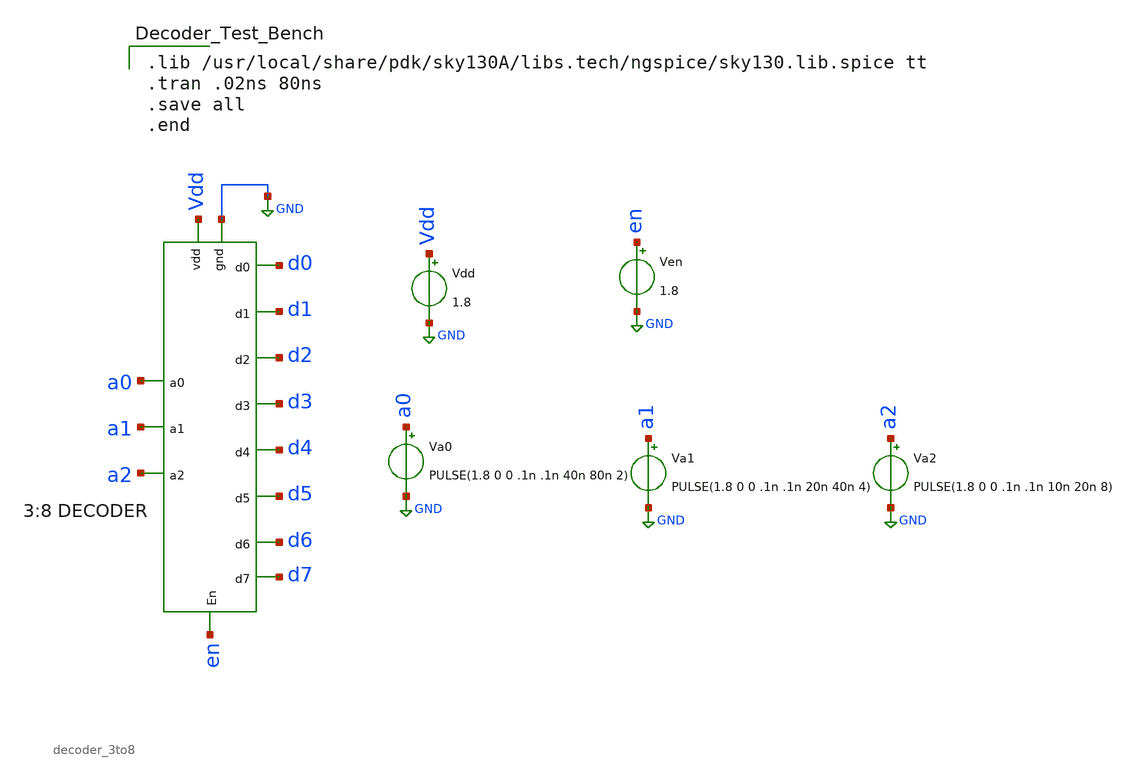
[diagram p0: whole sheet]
** sch_path: Projects/Schematic_Design_and_Analysis_of_an_8-Word_8-Bit_Static_RAM_with_6T_Storage_Cells_using_SKY130PDK/assets/schematic/decoder_3to8_tb.sch
**.subckt decoder_3to8_tb
Vdd Vdd GND 1.8
Va0 a0 GND PULSE(1.8 0 0 .1n .1n 40n 80n 2)
Va1 a1 GND PULSE(1.8 0 0 .1n .1n 20n 40n 4)
Va2 a2 GND PULSE(1.8 0 0 .1n .1n 10n 20n 8)
x1 d0 d1 d2 d3 d4 d5 d6 d7 Vdd GND en a0 a1 a2 decoder_3to8
Ven en GND 1.8
**** begin user architecture code

.lib /usr/local/share/pdk/sky130A/libs.tech/ngspice/sky130.lib.spice tt
.tran .02ns 80ns
.save all
.end

**** end user architecture code
**.ends

* expanding   symbol:  decoder_3to8.sym # of pins=14
** sym_path: Projects/Schematic_Design_and_Analysis_of_an_8-Word_8-Bit_Static_RAM_with_6T_Storage_Cells_using_SKY130PDK/assets/schematic/decoder_3to8.sym
** sch_path: Projects/Schematic_Design_and_Analysis_of_an_8-Word_8-Bit_Static_RAM_with_6T_Storage_Cells_using_SKY130PDK/assets/schematic/decoder_3to8.sch
.subckt decoder_3to8 d0 d1 d2 d3 d4 d5 d6 d7 vdd gnd En a0 a1 a2
*.ipin a0
*.ipin a1
*.ipin a2
*.opin d0
*.ipin vdd
*.ipin gnd
*.ipin En
*.opin d1
*.opin d2
*.opin d3
*.opin d4
*.opin d5
*.opin d6
*.opin d7
XM25 net1 a2 gnd gnd sky130_fd_pr__nfet_01v8 L=0.15 W=1 nf=1 ad='int((nf+1)/2) * W/nf * 0.29' as='int((nf+2)/2) * W/nf * 0.29'
+ pd='2*int((nf+1)/2) * (W/nf + 0.29)' ps='2*int((nf+2)/2) * (W/nf + 0.29)' nrd='0.29 / W' nrs='0.29 / W'
+ sa=0 sb=0 sd=0 mult=1 m=1
XM26 net1 a2 vdd vdd sky130_fd_pr__pfet_01v8 L=0.15 W=2 nf=1 ad='int((nf+1)/2) * W/nf * 0.29' as='int((nf+2)/2) * W/nf * 0.29'
+ pd='2*int((nf+1)/2) * (W/nf + 0.29)' ps='2*int((nf+2)/2) * (W/nf + 0.29)' nrd='0.29 / W' nrs='0.29 / W'
+ sa=0 sb=0 sd=0 mult=1 m=1
XM28 net2 a1 vdd vdd sky130_fd_pr__pfet_01v8 L=0.15 W=2 nf=1 ad='int((nf+1)/2) * W/nf * 0.29' as='int((nf+2)/2) * W/nf * 0.29'
+ pd='2*int((nf+1)/2) * (W/nf + 0.29)' ps='2*int((nf+2)/2) * (W/nf + 0.29)' nrd='0.29 / W' nrs='0.29 / W'
+ sa=0 sb=0 sd=0 mult=1 m=1
XM30 net3 a0 vdd vdd sky130_fd_pr__pfet_01v8 L=0.15 W=2 nf=1 ad='int((nf+1)/2) * W/nf * 0.29' as='int((nf+2)/2) * W/nf * 0.29'
+ pd='2*int((nf+1)/2) * (W/nf + 0.29)' ps='2*int((nf+2)/2) * (W/nf + 0.29)' nrd='0.29 / W' nrs='0.29 / W'
+ sa=0 sb=0 sd=0 mult=1 m=1
XM27 net2 a1 gnd gnd sky130_fd_pr__nfet_01v8 L=0.15 W=1 nf=1 ad='int((nf+1)/2) * W/nf * 0.29' as='int((nf+2)/2) * W/nf * 0.29'
+ pd='2*int((nf+1)/2) * (W/nf + 0.29)' ps='2*int((nf+2)/2) * (W/nf + 0.29)' nrd='0.29 / W' nrs='0.29 / W'
+ sa=0 sb=0 sd=0 mult=1 m=1
XM29 net3 a0 gnd gnd sky130_fd_pr__nfet_01v8 L=0.15 W=1 nf=1 ad='int((nf+1)/2) * W/nf * 0.29' as='int((nf+2)/2) * W/nf * 0.29'
+ pd='2*int((nf+1)/2) * (W/nf + 0.29)' ps='2*int((nf+2)/2) * (W/nf + 0.29)' nrd='0.29 / W' nrs='0.29 / W'
+ sa=0 sb=0 sd=0 mult=1 m=1
XM1 net5 gnd vdd vdd sky130_fd_pr__pfet_01v8 L=0.15 W=2 nf=1 ad='int((nf+1)/2) * W/nf * 0.29' as='int((nf+2)/2) * W/nf * 0.29'
+ pd='2*int((nf+1)/2) * (W/nf + 0.29)' ps='2*int((nf+2)/2) * (W/nf + 0.29)' nrd='0.29 / W' nrs='0.29 / W'
+ sa=0 sb=0 sd=0 mult=1 m=1
XM2 net5 En net4 gnd sky130_fd_pr__nfet_01v8 L=0.15 W=3 nf=1 ad='int((nf+1)/2) * W/nf * 0.29' as='int((nf+2)/2) * W/nf * 0.29'
+ pd='2*int((nf+1)/2) * (W/nf + 0.29)' ps='2*int((nf+2)/2) * (W/nf + 0.29)' nrd='0.29 / W' nrs='0.29 / W'
+ sa=0 sb=0 sd=0 mult=1 m=1
XM3 net4 net1 net6 gnd sky130_fd_pr__nfet_01v8 L=0.15 W=3 nf=1 ad='int((nf+1)/2) * W/nf * 0.29' as='int((nf+2)/2) * W/nf * 0.29'
+ pd='2*int((nf+1)/2) * (W/nf + 0.29)' ps='2*int((nf+2)/2) * (W/nf + 0.29)' nrd='0.29 / W' nrs='0.29 / W'
+ sa=0 sb=0 sd=0 mult=1 m=1
XM4 net6 net2 gnd gnd sky130_fd_pr__nfet_01v8 L=0.15 W=3 nf=1 ad='int((nf+1)/2) * W/nf * 0.29' as='int((nf+2)/2) * W/nf * 0.29'
+ pd='2*int((nf+1)/2) * (W/nf + 0.29)' ps='2*int((nf+2)/2) * (W/nf + 0.29)' nrd='0.29 / W' nrs='0.29 / W'
+ sa=0 sb=0 sd=0 mult=1 m=1
XM5 net8 gnd vdd vdd sky130_fd_pr__pfet_01v8 L=0.15 W=2 nf=1 ad='int((nf+1)/2) * W/nf * 0.29' as='int((nf+2)/2) * W/nf * 0.29'
+ pd='2*int((nf+1)/2) * (W/nf + 0.29)' ps='2*int((nf+2)/2) * (W/nf + 0.29)' nrd='0.29 / W' nrs='0.29 / W'
+ sa=0 sb=0 sd=0 mult=1 m=1
XM6 net8 En net7 gnd sky130_fd_pr__nfet_01v8 L=0.15 W=3 nf=1 ad='int((nf+1)/2) * W/nf * 0.29' as='int((nf+2)/2) * W/nf * 0.29'
+ pd='2*int((nf+1)/2) * (W/nf + 0.29)' ps='2*int((nf+2)/2) * (W/nf + 0.29)' nrd='0.29 / W' nrs='0.29 / W'
+ sa=0 sb=0 sd=0 mult=1 m=1
XM7 net7 a2 net9 gnd sky130_fd_pr__nfet_01v8 L=0.15 W=3 nf=1 ad='int((nf+1)/2) * W/nf * 0.29' as='int((nf+2)/2) * W/nf * 0.29'
+ pd='2*int((nf+1)/2) * (W/nf + 0.29)' ps='2*int((nf+2)/2) * (W/nf + 0.29)' nrd='0.29 / W' nrs='0.29 / W'
+ sa=0 sb=0 sd=0 mult=1 m=1
XM8 net9 net2 gnd gnd sky130_fd_pr__nfet_01v8 L=0.15 W=3 nf=1 ad='int((nf+1)/2) * W/nf * 0.29' as='int((nf+2)/2) * W/nf * 0.29'
+ pd='2*int((nf+1)/2) * (W/nf + 0.29)' ps='2*int((nf+2)/2) * (W/nf + 0.29)' nrd='0.29 / W' nrs='0.29 / W'
+ sa=0 sb=0 sd=0 mult=1 m=1
XM9 net11 gnd vdd vdd sky130_fd_pr__pfet_01v8 L=0.15 W=2 nf=1 ad='int((nf+1)/2) * W/nf * 0.29' as='int((nf+2)/2) * W/nf * 0.29'
+ pd='2*int((nf+1)/2) * (W/nf + 0.29)' ps='2*int((nf+2)/2) * (W/nf + 0.29)' nrd='0.29 / W' nrs='0.29 / W'
+ sa=0 sb=0 sd=0 mult=1 m=1
XM10 net11 En net10 gnd sky130_fd_pr__nfet_01v8 L=0.15 W=3 nf=1 ad='int((nf+1)/2) * W/nf * 0.29' as='int((nf+2)/2) * W/nf * 0.29'
+ pd='2*int((nf+1)/2) * (W/nf + 0.29)' ps='2*int((nf+2)/2) * (W/nf + 0.29)' nrd='0.29 / W' nrs='0.29 / W'
+ sa=0 sb=0 sd=0 mult=1 m=1
XM11 net10 net1 net12 gnd sky130_fd_pr__nfet_01v8 L=0.15 W=3 nf=1 ad='int((nf+1)/2) * W/nf * 0.29' as='int((nf+2)/2) * W/nf * 0.29'
+ pd='2*int((nf+1)/2) * (W/nf + 0.29)' ps='2*int((nf+2)/2) * (W/nf + 0.29)' nrd='0.29 / W' nrs='0.29 / W'
+ sa=0 sb=0 sd=0 mult=1 m=1
XM12 net12 a1 gnd gnd sky130_fd_pr__nfet_01v8 L=0.15 W=3 nf=1 ad='int((nf+1)/2) * W/nf * 0.29' as='int((nf+2)/2) * W/nf * 0.29'
+ pd='2*int((nf+1)/2) * (W/nf + 0.29)' ps='2*int((nf+2)/2) * (W/nf + 0.29)' nrd='0.29 / W' nrs='0.29 / W'
+ sa=0 sb=0 sd=0 mult=1 m=1
XM13 net14 gnd vdd vdd sky130_fd_pr__pfet_01v8 L=0.15 W=2 nf=1 ad='int((nf+1)/2) * W/nf * 0.29' as='int((nf+2)/2) * W/nf * 0.29'
+ pd='2*int((nf+1)/2) * (W/nf + 0.29)' ps='2*int((nf+2)/2) * (W/nf + 0.29)' nrd='0.29 / W' nrs='0.29 / W'
+ sa=0 sb=0 sd=0 mult=1 m=1
XM14 net14 En net13 gnd sky130_fd_pr__nfet_01v8 L=0.15 W=3 nf=1 ad='int((nf+1)/2) * W/nf * 0.29' as='int((nf+2)/2) * W/nf * 0.29'
+ pd='2*int((nf+1)/2) * (W/nf + 0.29)' ps='2*int((nf+2)/2) * (W/nf + 0.29)' nrd='0.29 / W' nrs='0.29 / W'
+ sa=0 sb=0 sd=0 mult=1 m=1
XM15 net13 a2 net15 gnd sky130_fd_pr__nfet_01v8 L=0.15 W=3 nf=1 ad='int((nf+1)/2) * W/nf * 0.29' as='int((nf+2)/2) * W/nf * 0.29'
+ pd='2*int((nf+1)/2) * (W/nf + 0.29)' ps='2*int((nf+2)/2) * (W/nf + 0.29)' nrd='0.29 / W' nrs='0.29 / W'
+ sa=0 sb=0 sd=0 mult=1 m=1
XM16 net15 a1 gnd gnd sky130_fd_pr__nfet_01v8 L=0.15 W=3 nf=1 ad='int((nf+1)/2) * W/nf * 0.29' as='int((nf+2)/2) * W/nf * 0.29'
+ pd='2*int((nf+1)/2) * (W/nf + 0.29)' ps='2*int((nf+2)/2) * (W/nf + 0.29)' nrd='0.29 / W' nrs='0.29 / W'
+ sa=0 sb=0 sd=0 mult=1 m=1
XM17 net17 gnd vdd vdd sky130_fd_pr__pfet_01v8 L=0.15 W=2 nf=1 ad='int((nf+1)/2) * W/nf * 0.29' as='int((nf+2)/2) * W/nf * 0.29'
+ pd='2*int((nf+1)/2) * (W/nf + 0.29)' ps='2*int((nf+2)/2) * (W/nf + 0.29)' nrd='0.29 / W' nrs='0.29 / W'
+ sa=0 sb=0 sd=0 mult=1 m=1
XM18 net17 net3 net16 gnd sky130_fd_pr__nfet_01v8 L=0.15 W=2 nf=1 ad='int((nf+1)/2) * W/nf * 0.29' as='int((nf+2)/2) * W/nf * 0.29'
+ pd='2*int((nf+1)/2) * (W/nf + 0.29)' ps='2*int((nf+2)/2) * (W/nf + 0.29)' nrd='0.29 / W' nrs='0.29 / W'
+ sa=0 sb=0 sd=0 mult=1 m=1
XM20 net19 gnd vdd vdd sky130_fd_pr__pfet_01v8 L=0.15 W=2 nf=1 ad='int((nf+1)/2) * W/nf * 0.29' as='int((nf+2)/2) * W/nf * 0.29'
+ pd='2*int((nf+1)/2) * (W/nf + 0.29)' ps='2*int((nf+2)/2) * (W/nf + 0.29)' nrd='0.29 / W' nrs='0.29 / W'
+ sa=0 sb=0 sd=0 mult=1 m=1
XM23 net21 gnd vdd vdd sky130_fd_pr__pfet_01v8 L=0.15 W=2 nf=1 ad='int((nf+1)/2) * W/nf * 0.29' as='int((nf+2)/2) * W/nf * 0.29'
+ pd='2*int((nf+1)/2) * (W/nf + 0.29)' ps='2*int((nf+2)/2) * (W/nf + 0.29)' nrd='0.29 / W' nrs='0.29 / W'
+ sa=0 sb=0 sd=0 mult=1 m=1
XM32 net23 gnd vdd vdd sky130_fd_pr__pfet_01v8 L=0.15 W=2 nf=1 ad='int((nf+1)/2) * W/nf * 0.29' as='int((nf+2)/2) * W/nf * 0.29'
+ pd='2*int((nf+1)/2) * (W/nf + 0.29)' ps='2*int((nf+2)/2) * (W/nf + 0.29)' nrd='0.29 / W' nrs='0.29 / W'
+ sa=0 sb=0 sd=0 mult=1 m=1
XM35 net25 gnd vdd vdd sky130_fd_pr__pfet_01v8 L=0.15 W=2 nf=1 ad='int((nf+1)/2) * W/nf * 0.29' as='int((nf+2)/2) * W/nf * 0.29'
+ pd='2*int((nf+1)/2) * (W/nf + 0.29)' ps='2*int((nf+2)/2) * (W/nf + 0.29)' nrd='0.29 / W' nrs='0.29 / W'
+ sa=0 sb=0 sd=0 mult=1 m=1
XM38 net27 gnd vdd vdd sky130_fd_pr__pfet_01v8 L=0.15 W=2 nf=1 ad='int((nf+1)/2) * W/nf * 0.29' as='int((nf+2)/2) * W/nf * 0.29'
+ pd='2*int((nf+1)/2) * (W/nf + 0.29)' ps='2*int((nf+2)/2) * (W/nf + 0.29)' nrd='0.29 / W' nrs='0.29 / W'
+ sa=0 sb=0 sd=0 mult=1 m=1
XM41 net29 gnd vdd vdd sky130_fd_pr__pfet_01v8 L=0.15 W=2 nf=1 ad='int((nf+1)/2) * W/nf * 0.29' as='int((nf+2)/2) * W/nf * 0.29'
+ pd='2*int((nf+1)/2) * (W/nf + 0.29)' ps='2*int((nf+2)/2) * (W/nf + 0.29)' nrd='0.29 / W' nrs='0.29 / W'
+ sa=0 sb=0 sd=0 mult=1 m=1
XM44 net31 gnd vdd vdd sky130_fd_pr__pfet_01v8 L=0.15 W=2 nf=1 ad='int((nf+1)/2) * W/nf * 0.29' as='int((nf+2)/2) * W/nf * 0.29'
+ pd='2*int((nf+1)/2) * (W/nf + 0.29)' ps='2*int((nf+2)/2) * (W/nf + 0.29)' nrd='0.29 / W' nrs='0.29 / W'
+ sa=0 sb=0 sd=0 mult=1 m=1
XM47 d0 net17 vdd vdd sky130_fd_pr__pfet_01v8 L=0.15 W=2 nf=1 ad='int((nf+1)/2) * W/nf * 0.29' as='int((nf+2)/2) * W/nf * 0.29'
+ pd='2*int((nf+1)/2) * (W/nf + 0.29)' ps='2*int((nf+2)/2) * (W/nf + 0.29)' nrd='0.29 / W' nrs='0.29 / W'
+ sa=0 sb=0 sd=0 mult=1 m=1
XM48 d0 net17 gnd gnd sky130_fd_pr__nfet_01v8 L=0.15 W=1 nf=1 ad='int((nf+1)/2) * W/nf * 0.29' as='int((nf+2)/2) * W/nf * 0.29'
+ pd='2*int((nf+1)/2) * (W/nf + 0.29)' ps='2*int((nf+2)/2) * (W/nf + 0.29)' nrd='0.29 / W' nrs='0.29 / W'
+ sa=0 sb=0 sd=0 mult=1 m=1
XM19 net16 net32 gnd gnd sky130_fd_pr__nfet_01v8 L=0.15 W=2 nf=1 ad='int((nf+1)/2) * W/nf * 0.29' as='int((nf+2)/2) * W/nf * 0.29'
+ pd='2*int((nf+1)/2) * (W/nf + 0.29)' ps='2*int((nf+2)/2) * (W/nf + 0.29)' nrd='0.29 / W' nrs='0.29 / W'
+ sa=0 sb=0 sd=0 mult=1 m=1
XM21 net19 net3 net18 gnd sky130_fd_pr__nfet_01v8 L=0.15 W=2 nf=1 ad='int((nf+1)/2) * W/nf * 0.29' as='int((nf+2)/2) * W/nf * 0.29'
+ pd='2*int((nf+1)/2) * (W/nf + 0.29)' ps='2*int((nf+2)/2) * (W/nf + 0.29)' nrd='0.29 / W' nrs='0.29 / W'
+ sa=0 sb=0 sd=0 mult=1 m=1
XM22 net18 net33 gnd gnd sky130_fd_pr__nfet_01v8 L=0.15 W=2 nf=1 ad='int((nf+1)/2) * W/nf * 0.29' as='int((nf+2)/2) * W/nf * 0.29'
+ pd='2*int((nf+1)/2) * (W/nf + 0.29)' ps='2*int((nf+2)/2) * (W/nf + 0.29)' nrd='0.29 / W' nrs='0.29 / W'
+ sa=0 sb=0 sd=0 mult=1 m=1
XM24 net21 net3 net20 gnd sky130_fd_pr__nfet_01v8 L=0.15 W=2 nf=1 ad='int((nf+1)/2) * W/nf * 0.29' as='int((nf+2)/2) * W/nf * 0.29'
+ pd='2*int((nf+1)/2) * (W/nf + 0.29)' ps='2*int((nf+2)/2) * (W/nf + 0.29)' nrd='0.29 / W' nrs='0.29 / W'
+ sa=0 sb=0 sd=0 mult=1 m=1
XM31 net20 net34 gnd gnd sky130_fd_pr__nfet_01v8 L=0.15 W=2 nf=1 ad='int((nf+1)/2) * W/nf * 0.29' as='int((nf+2)/2) * W/nf * 0.29'
+ pd='2*int((nf+1)/2) * (W/nf + 0.29)' ps='2*int((nf+2)/2) * (W/nf + 0.29)' nrd='0.29 / W' nrs='0.29 / W'
+ sa=0 sb=0 sd=0 mult=1 m=1
XM33 net23 net3 net22 gnd sky130_fd_pr__nfet_01v8 L=0.15 W=2 nf=1 ad='int((nf+1)/2) * W/nf * 0.29' as='int((nf+2)/2) * W/nf * 0.29'
+ pd='2*int((nf+1)/2) * (W/nf + 0.29)' ps='2*int((nf+2)/2) * (W/nf + 0.29)' nrd='0.29 / W' nrs='0.29 / W'
+ sa=0 sb=0 sd=0 mult=1 m=1
XM34 net22 net35 gnd gnd sky130_fd_pr__nfet_01v8 L=0.15 W=2 nf=1 ad='int((nf+1)/2) * W/nf * 0.29' as='int((nf+2)/2) * W/nf * 0.29'
+ pd='2*int((nf+1)/2) * (W/nf + 0.29)' ps='2*int((nf+2)/2) * (W/nf + 0.29)' nrd='0.29 / W' nrs='0.29 / W'
+ sa=0 sb=0 sd=0 mult=1 m=1
XM36 net25 a0 net24 gnd sky130_fd_pr__nfet_01v8 L=0.15 W=2 nf=1 ad='int((nf+1)/2) * W/nf * 0.29' as='int((nf+2)/2) * W/nf * 0.29'
+ pd='2*int((nf+1)/2) * (W/nf + 0.29)' ps='2*int((nf+2)/2) * (W/nf + 0.29)' nrd='0.29 / W' nrs='0.29 / W'
+ sa=0 sb=0 sd=0 mult=1 m=1
XM37 net24 net32 gnd gnd sky130_fd_pr__nfet_01v8 L=0.15 W=2 nf=1 ad='int((nf+1)/2) * W/nf * 0.29' as='int((nf+2)/2) * W/nf * 0.29'
+ pd='2*int((nf+1)/2) * (W/nf + 0.29)' ps='2*int((nf+2)/2) * (W/nf + 0.29)' nrd='0.29 / W' nrs='0.29 / W'
+ sa=0 sb=0 sd=0 mult=1 m=1
XM39 net27 a0 net26 gnd sky130_fd_pr__nfet_01v8 L=0.15 W=2 nf=1 ad='int((nf+1)/2) * W/nf * 0.29' as='int((nf+2)/2) * W/nf * 0.29'
+ pd='2*int((nf+1)/2) * (W/nf + 0.29)' ps='2*int((nf+2)/2) * (W/nf + 0.29)' nrd='0.29 / W' nrs='0.29 / W'
+ sa=0 sb=0 sd=0 mult=1 m=1
XM40 net26 net33 gnd gnd sky130_fd_pr__nfet_01v8 L=0.15 W=2 nf=1 ad='int((nf+1)/2) * W/nf * 0.29' as='int((nf+2)/2) * W/nf * 0.29'
+ pd='2*int((nf+1)/2) * (W/nf + 0.29)' ps='2*int((nf+2)/2) * (W/nf + 0.29)' nrd='0.29 / W' nrs='0.29 / W'
+ sa=0 sb=0 sd=0 mult=1 m=1
XM42 net29 a0 net28 gnd sky130_fd_pr__nfet_01v8 L=0.15 W=2 nf=1 ad='int((nf+1)/2) * W/nf * 0.29' as='int((nf+2)/2) * W/nf * 0.29'
+ pd='2*int((nf+1)/2) * (W/nf + 0.29)' ps='2*int((nf+2)/2) * (W/nf + 0.29)' nrd='0.29 / W' nrs='0.29 / W'
+ sa=0 sb=0 sd=0 mult=1 m=1
XM43 net28 net34 gnd gnd sky130_fd_pr__nfet_01v8 L=0.15 W=2 nf=1 ad='int((nf+1)/2) * W/nf * 0.29' as='int((nf+2)/2) * W/nf * 0.29'
+ pd='2*int((nf+1)/2) * (W/nf + 0.29)' ps='2*int((nf+2)/2) * (W/nf + 0.29)' nrd='0.29 / W' nrs='0.29 / W'
+ sa=0 sb=0 sd=0 mult=1 m=1
XM45 net31 a0 net30 gnd sky130_fd_pr__nfet_01v8 L=0.15 W=2 nf=1 ad='int((nf+1)/2) * W/nf * 0.29' as='int((nf+2)/2) * W/nf * 0.29'
+ pd='2*int((nf+1)/2) * (W/nf + 0.29)' ps='2*int((nf+2)/2) * (W/nf + 0.29)' nrd='0.29 / W' nrs='0.29 / W'
+ sa=0 sb=0 sd=0 mult=1 m=1
XM46 net30 net35 gnd gnd sky130_fd_pr__nfet_01v8 L=0.15 W=2 nf=1 ad='int((nf+1)/2) * W/nf * 0.29' as='int((nf+2)/2) * W/nf * 0.29'
+ pd='2*int((nf+1)/2) * (W/nf + 0.29)' ps='2*int((nf+2)/2) * (W/nf + 0.29)' nrd='0.29 / W' nrs='0.29 / W'
+ sa=0 sb=0 sd=0 mult=1 m=1
XM49 d1 net19 vdd vdd sky130_fd_pr__pfet_01v8 L=0.15 W=2 nf=1 ad='int((nf+1)/2) * W/nf * 0.29' as='int((nf+2)/2) * W/nf * 0.29'
+ pd='2*int((nf+1)/2) * (W/nf + 0.29)' ps='2*int((nf+2)/2) * (W/nf + 0.29)' nrd='0.29 / W' nrs='0.29 / W'
+ sa=0 sb=0 sd=0 mult=1 m=1
XM50 d1 net19 gnd gnd sky130_fd_pr__nfet_01v8 L=0.15 W=1 nf=1 ad='int((nf+1)/2) * W/nf * 0.29' as='int((nf+2)/2) * W/nf * 0.29'
+ pd='2*int((nf+1)/2) * (W/nf + 0.29)' ps='2*int((nf+2)/2) * (W/nf + 0.29)' nrd='0.29 / W' nrs='0.29 / W'
+ sa=0 sb=0 sd=0 mult=1 m=1
XM51 d2 net21 vdd vdd sky130_fd_pr__pfet_01v8 L=0.15 W=2 nf=1 ad='int((nf+1)/2) * W/nf * 0.29' as='int((nf+2)/2) * W/nf * 0.29'
+ pd='2*int((nf+1)/2) * (W/nf + 0.29)' ps='2*int((nf+2)/2) * (W/nf + 0.29)' nrd='0.29 / W' nrs='0.29 / W'
+ sa=0 sb=0 sd=0 mult=1 m=1
XM52 d2 net21 gnd gnd sky130_fd_pr__nfet_01v8 L=0.15 W=1 nf=1 ad='int((nf+1)/2) * W/nf * 0.29' as='int((nf+2)/2) * W/nf * 0.29'
+ pd='2*int((nf+1)/2) * (W/nf + 0.29)' ps='2*int((nf+2)/2) * (W/nf + 0.29)' nrd='0.29 / W' nrs='0.29 / W'
+ sa=0 sb=0 sd=0 mult=1 m=1
XM53 d3 net23 vdd vdd sky130_fd_pr__pfet_01v8 L=0.15 W=2 nf=1 ad='int((nf+1)/2) * W/nf * 0.29' as='int((nf+2)/2) * W/nf * 0.29'
+ pd='2*int((nf+1)/2) * (W/nf + 0.29)' ps='2*int((nf+2)/2) * (W/nf + 0.29)' nrd='0.29 / W' nrs='0.29 / W'
+ sa=0 sb=0 sd=0 mult=1 m=1
XM54 d3 net23 gnd gnd sky130_fd_pr__nfet_01v8 L=0.15 W=1 nf=1 ad='int((nf+1)/2) * W/nf * 0.29' as='int((nf+2)/2) * W/nf * 0.29'
+ pd='2*int((nf+1)/2) * (W/nf + 0.29)' ps='2*int((nf+2)/2) * (W/nf + 0.29)' nrd='0.29 / W' nrs='0.29 / W'
+ sa=0 sb=0 sd=0 mult=1 m=1
XM55 d4 net25 vdd vdd sky130_fd_pr__pfet_01v8 L=0.15 W=2 nf=1 ad='int((nf+1)/2) * W/nf * 0.29' as='int((nf+2)/2) * W/nf * 0.29'
+ pd='2*int((nf+1)/2) * (W/nf + 0.29)' ps='2*int((nf+2)/2) * (W/nf + 0.29)' nrd='0.29 / W' nrs='0.29 / W'
+ sa=0 sb=0 sd=0 mult=1 m=1
XM56 d4 net25 gnd gnd sky130_fd_pr__nfet_01v8 L=0.15 W=1 nf=1 ad='int((nf+1)/2) * W/nf * 0.29' as='int((nf+2)/2) * W/nf * 0.29'
+ pd='2*int((nf+1)/2) * (W/nf + 0.29)' ps='2*int((nf+2)/2) * (W/nf + 0.29)' nrd='0.29 / W' nrs='0.29 / W'
+ sa=0 sb=0 sd=0 mult=1 m=1
XM57 d5 net27 vdd vdd sky130_fd_pr__pfet_01v8 L=0.15 W=2 nf=1 ad='int((nf+1)/2) * W/nf * 0.29' as='int((nf+2)/2) * W/nf * 0.29'
+ pd='2*int((nf+1)/2) * (W/nf + 0.29)' ps='2*int((nf+2)/2) * (W/nf + 0.29)' nrd='0.29 / W' nrs='0.29 / W'
+ sa=0 sb=0 sd=0 mult=1 m=1
XM58 d5 net27 gnd gnd sky130_fd_pr__nfet_01v8 L=0.15 W=1 nf=1 ad='int((nf+1)/2) * W/nf * 0.29' as='int((nf+2)/2) * W/nf * 0.29'
+ pd='2*int((nf+1)/2) * (W/nf + 0.29)' ps='2*int((nf+2)/2) * (W/nf + 0.29)' nrd='0.29 / W' nrs='0.29 / W'
+ sa=0 sb=0 sd=0 mult=1 m=1
XM59 d6 net29 vdd vdd sky130_fd_pr__pfet_01v8 L=0.15 W=2 nf=1 ad='int((nf+1)/2) * W/nf * 0.29' as='int((nf+2)/2) * W/nf * 0.29'
+ pd='2*int((nf+1)/2) * (W/nf + 0.29)' ps='2*int((nf+2)/2) * (W/nf + 0.29)' nrd='0.29 / W' nrs='0.29 / W'
+ sa=0 sb=0 sd=0 mult=1 m=1
XM60 d6 net29 gnd gnd sky130_fd_pr__nfet_01v8 L=0.15 W=1 nf=1 ad='int((nf+1)/2) * W/nf * 0.29' as='int((nf+2)/2) * W/nf * 0.29'
+ pd='2*int((nf+1)/2) * (W/nf + 0.29)' ps='2*int((nf+2)/2) * (W/nf + 0.29)' nrd='0.29 / W' nrs='0.29 / W'
+ sa=0 sb=0 sd=0 mult=1 m=1
XM61 d7 net31 vdd vdd sky130_fd_pr__pfet_01v8 L=0.15 W=2 nf=1 ad='int((nf+1)/2) * W/nf * 0.29' as='int((nf+2)/2) * W/nf * 0.29'
+ pd='2*int((nf+1)/2) * (W/nf + 0.29)' ps='2*int((nf+2)/2) * (W/nf + 0.29)' nrd='0.29 / W' nrs='0.29 / W'
+ sa=0 sb=0 sd=0 mult=1 m=1
XM62 d7 net31 gnd gnd sky130_fd_pr__nfet_01v8 L=0.15 W=1 nf=1 ad='int((nf+1)/2) * W/nf * 0.29' as='int((nf+2)/2) * W/nf * 0.29'
+ pd='2*int((nf+1)/2) * (W/nf + 0.29)' ps='2*int((nf+2)/2) * (W/nf + 0.29)' nrd='0.29 / W' nrs='0.29 / W'
+ sa=0 sb=0 sd=0 mult=1 m=1
XM63 net32 net5 vdd vdd sky130_fd_pr__pfet_01v8 L=0.15 W=2 nf=1 ad='int((nf+1)/2) * W/nf * 0.29' as='int((nf+2)/2) * W/nf * 0.29'
+ pd='2*int((nf+1)/2) * (W/nf + 0.29)' ps='2*int((nf+2)/2) * (W/nf + 0.29)' nrd='0.29 / W' nrs='0.29 / W'
+ sa=0 sb=0 sd=0 mult=1 m=1
XM64 net32 net5 gnd gnd sky130_fd_pr__nfet_01v8 L=0.15 W=1 nf=1 ad='int((nf+1)/2) * W/nf * 0.29' as='int((nf+2)/2) * W/nf * 0.29'
+ pd='2*int((nf+1)/2) * (W/nf + 0.29)' ps='2*int((nf+2)/2) * (W/nf + 0.29)' nrd='0.29 / W' nrs='0.29 / W'
+ sa=0 sb=0 sd=0 mult=1 m=1
XM65 net33 net8 vdd vdd sky130_fd_pr__pfet_01v8 L=0.15 W=2 nf=1 ad='int((nf+1)/2) * W/nf * 0.29' as='int((nf+2)/2) * W/nf * 0.29'
+ pd='2*int((nf+1)/2) * (W/nf + 0.29)' ps='2*int((nf+2)/2) * (W/nf + 0.29)' nrd='0.29 / W' nrs='0.29 / W'
+ sa=0 sb=0 sd=0 mult=1 m=1
XM66 net33 net8 gnd gnd sky130_fd_pr__nfet_01v8 L=0.15 W=1 nf=1 ad='int((nf+1)/2) * W/nf * 0.29' as='int((nf+2)/2) * W/nf * 0.29'
+ pd='2*int((nf+1)/2) * (W/nf + 0.29)' ps='2*int((nf+2)/2) * (W/nf + 0.29)' nrd='0.29 / W' nrs='0.29 / W'
+ sa=0 sb=0 sd=0 mult=1 m=1
XM67 net34 net11 vdd vdd sky130_fd_pr__pfet_01v8 L=0.15 W=2 nf=1 ad='int((nf+1)/2) * W/nf * 0.29' as='int((nf+2)/2) * W/nf * 0.29'
+ pd='2*int((nf+1)/2) * (W/nf + 0.29)' ps='2*int((nf+2)/2) * (W/nf + 0.29)' nrd='0.29 / W' nrs='0.29 / W'
+ sa=0 sb=0 sd=0 mult=1 m=1
XM68 net34 net11 gnd gnd sky130_fd_pr__nfet_01v8 L=0.15 W=1 nf=1 ad='int((nf+1)/2) * W/nf * 0.29' as='int((nf+2)/2) * W/nf * 0.29'
+ pd='2*int((nf+1)/2) * (W/nf + 0.29)' ps='2*int((nf+2)/2) * (W/nf + 0.29)' nrd='0.29 / W' nrs='0.29 / W'
+ sa=0 sb=0 sd=0 mult=1 m=1
XM69 net35 net14 vdd vdd sky130_fd_pr__pfet_01v8 L=0.15 W=2 nf=1 ad='int((nf+1)/2) * W/nf * 0.29' as='int((nf+2)/2) * W/nf * 0.29'
+ pd='2*int((nf+1)/2) * (W/nf + 0.29)' ps='2*int((nf+2)/2) * (W/nf + 0.29)' nrd='0.29 / W' nrs='0.29 / W'
+ sa=0 sb=0 sd=0 mult=1 m=1
XM70 net35 net14 gnd gnd sky130_fd_pr__nfet_01v8 L=0.15 W=1 nf=1 ad='int((nf+1)/2) * W/nf * 0.29' as='int((nf+2)/2) * W/nf * 0.29'
+ pd='2*int((nf+1)/2) * (W/nf + 0.29)' ps='2*int((nf+2)/2) * (W/nf + 0.29)' nrd='0.29 / W' nrs='0.29 / W'
+ sa=0 sb=0 sd=0 mult=1 m=1
.ends

.GLOBAL GND
.end
